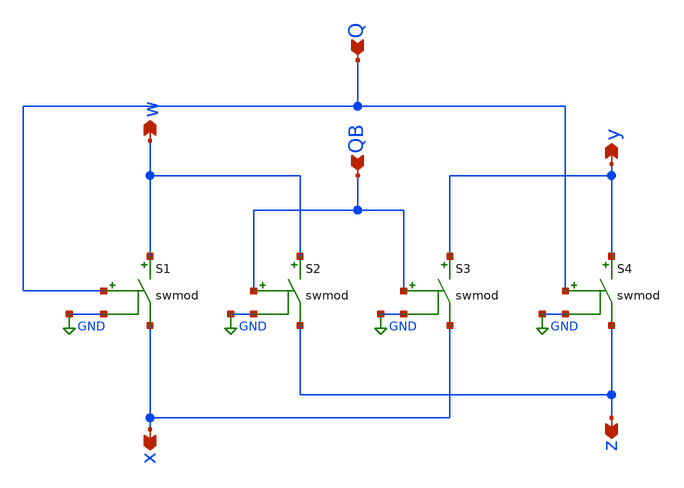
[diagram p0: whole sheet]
** sch_path: chopperid.sch
**.subckt chopperid Q QB w y x z
*.ipin Q
*.ipin QB
*.opin w
*.opin y
*.opin x
*.opin z
S1 w x Q GND swmod
S2 w z QB GND swmod
S3 y x QB GND swmod
S4 y z Q GND swmod
**.ends
.GLOBAL GND
.end
